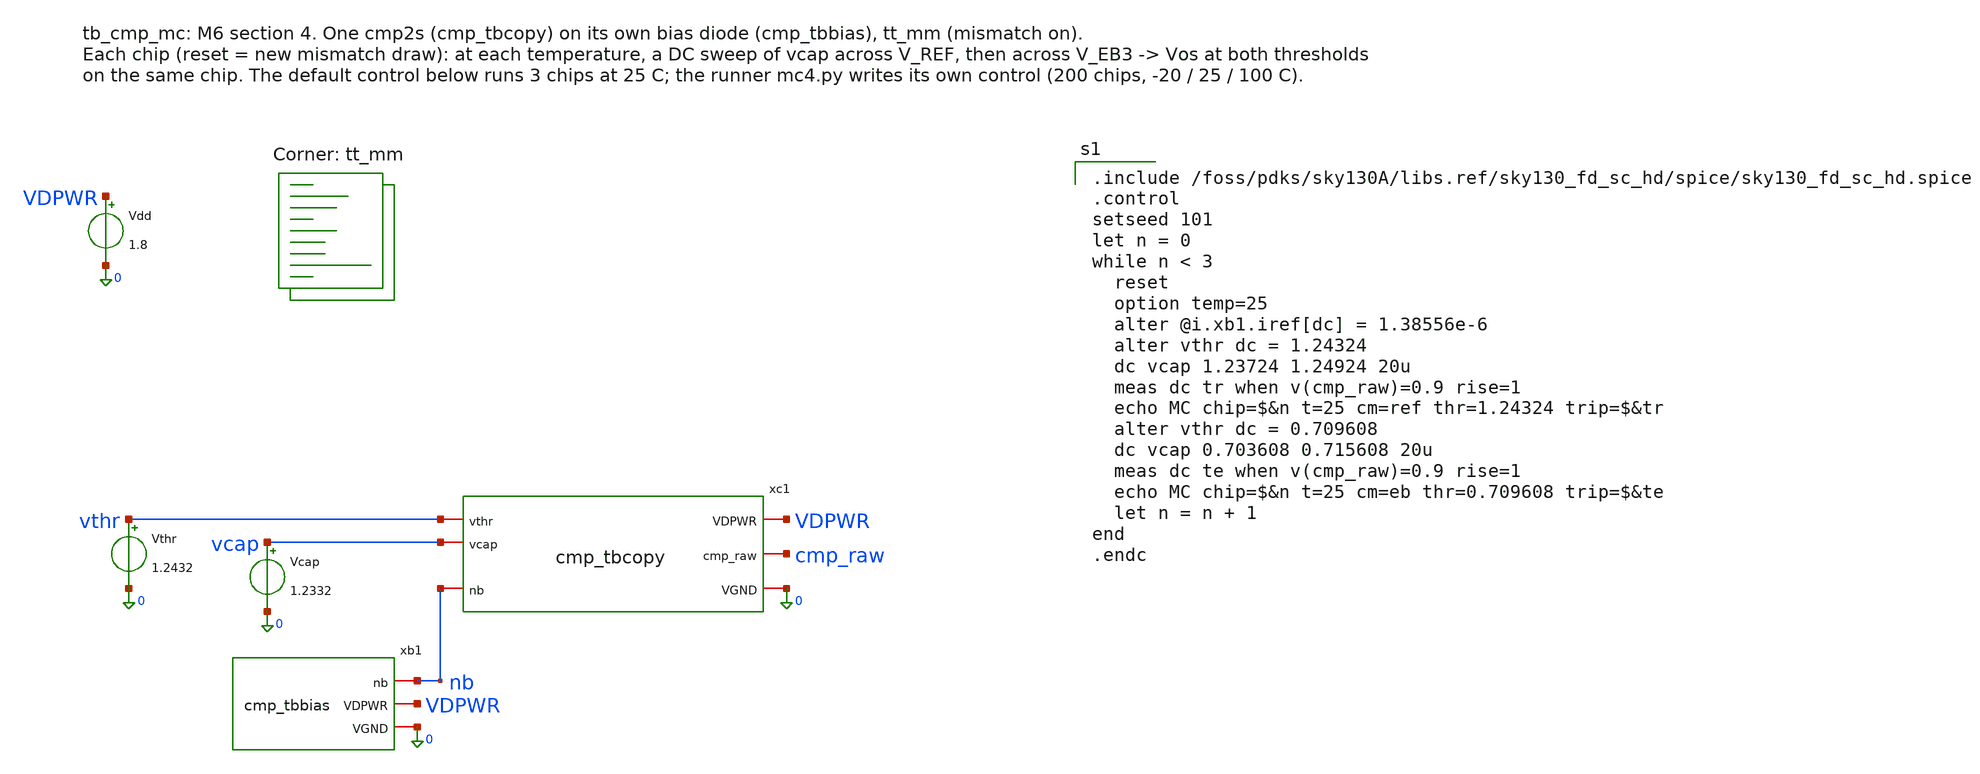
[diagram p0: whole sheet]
** sch_path: xschem/tb_cmp_mc.sch
**.subckt tb_cmp_mc
xc1 vthr vcap nb VDPWR cmp_raw 0 cmp_tbcopy
xb1 nb VDPWR 0 cmp_tbbias
Vthr vthr 0 1.2432
Vcap vcap 0 1.2332
Vdd VDPWR 0 1.8
**** begin user architecture code
.lib $::SKYWATER_MODELS/sky130.lib.spice tt_mm

.include /foss/pdks/sky130A/libs.ref/sky130_fd_sc_hd/spice/sky130_fd_sc_hd.spice
.control
setseed 101
let n = 0
while n < 3
  reset
  option temp=25
  alter @i.xb1.iref[dc] = 1.38556e-6
  alter vthr dc = 1.24324
  dc vcap 1.23724 1.24924 20u
  meas dc tr when v(cmp_raw)=0.9 rise=1
  echo MC chip=$&n t=25 cm=ref thr=1.24324 trip=$&tr
  alter vthr dc = 0.709608
  dc vcap 0.703608 0.715608 20u
  meas dc te when v(cmp_raw)=0.9 rise=1
  echo MC chip=$&n t=25 cm=eb thr=0.709608 trip=$&te
  let n = n + 1
end
.endc

**** end user architecture code
**.ends

* expanding   symbol:  cmp_tbcopy.sym # of pins=6
** sym_path: xschem/cmp_tbcopy.sym
** sch_path: xschem/cmp_tbcopy.sch
.subckt cmp_tbcopy vthr vcap nb VDPWR cmp_raw VGND
*.ipin vthr
*.ipin vcap
*.iopin nb
*.iopin VDPWR
*.opin cmp_raw
*.iopin VGND
x1 vthr vcap ib_cmp1 ib_cmp2 VDPWR cmp_raw VGND cmp2s
XMNB3 ib_cmp1 nb VGND VGND sky130_fd_pr__nfet_01v8 L=8 W=4 nf=1 ad='int((1 + 1)/2) * 4 / 1 * 0.29' as='int((1 + 2)/2) * 4 / 1 * 0.29'
+ pd='2*int((1 + 1)/2) * (4 / 1 + 0.29)' ps='2*int((1 + 2)/2) * (4 / 1 + 0.29)' nrd='0.29 / 4 ' nrs='0.29 / 4 '
+ sa=0 sb=0 sd=0 mult=4 m=4
XMNB4 ib_cmp2 nb VGND VGND sky130_fd_pr__nfet_01v8 L=8 W=4 nf=1 ad='int((1 + 1)/2) * 4 / 1 * 0.29' as='int((1 + 2)/2) * 4 / 1 * 0.29'
+ pd='2*int((1 + 1)/2) * (4 / 1 + 0.29)' ps='2*int((1 + 2)/2) * (4 / 1 + 0.29)' nrd='0.29 / 4 ' nrs='0.29 / 4 '
+ sa=0 sb=0 sd=0 mult=4 m=4
Cw1 ib_cmp1 VGND 40f m=1
Cw2 ib_cmp2 VGND 40f m=1
.ends


* expanding   symbol:  cmp_tbbias.sym # of pins=3
** sym_path: xschem/cmp_tbbias.sym
** sch_path: xschem/cmp_tbbias.sch
.subckt cmp_tbbias nb VDPWR VGND
*.iopin VDPWR
*.iopin nb
*.iopin VGND
Iref VDPWR nb 1.386u
XMNB1 nb nb VGND VGND sky130_fd_pr__nfet_01v8 L=8 W=4 nf=1 ad='int((1 + 1)/2) * 4 / 1 * 0.29' as='int((1 + 2)/2) * 4 / 1 * 0.29'
+ pd='2*int((1 + 1)/2) * (4 / 1 + 0.29)' ps='2*int((1 + 2)/2) * (4 / 1 + 0.29)' nrd='0.29 / 4 ' nrs='0.29 / 4 '
+ sa=0 sb=0 sd=0 mult=1 m=1
.ends


* expanding   symbol:  cmp2s.sym # of pins=7
** sym_path: xschem/cmp2s.sym
** sch_path: xschem/cmp2s.sch
.subckt cmp2s vthr vcap ib_cmp1 ib_cmp2 VDPWR cmp_raw VGND
*.iopin VDPWR
*.iopin VGND
*.ipin vthr
*.ipin vcap
*.iopin ib_cmp1
*.iopin ib_cmp2
*.opin cmp_raw
XM2a nd nd VDPWR VDPWR sky130_fd_pr__pfet_01v8_lvt L=4 W=4 nf=1 ad='int((1 + 1)/2) * 4 / 1 * 0.29' as='int((1 + 2)/2) * 4 / 1 * 0.29'
+ pd='2*int((1 + 1)/2) * (4 / 1 + 0.29)' ps='2*int((1 + 2)/2) * (4 / 1 + 0.29)' nrd='0.29 / 4 ' nrs='0.29 / 4 '
+ sa=0 sb=0 sd=0 mult=8 m=8
XM2b n1 nd VDPWR VDPWR sky130_fd_pr__pfet_01v8_lvt L=4 W=4 nf=1 ad='int((1 + 1)/2) * 4 / 1 * 0.29' as='int((1 + 2)/2) * 4 / 1 * 0.29'
+ pd='2*int((1 + 1)/2) * (4 / 1 + 0.29)' ps='2*int((1 + 2)/2) * (4 / 1 + 0.29)' nrd='0.29 / 4 ' nrs='0.29 / 4 '
+ sa=0 sb=0 sd=0 mult=8 m=8
XM1a nd vthr ib_cmp1 VGND sky130_fd_pr__nfet_01v8_lvt L=1.75 W=10 nf=1 ad='int((1 + 1)/2) * 10 / 1 * 0.29'
+ as='int((1 + 2)/2) * 10 / 1 * 0.29' pd='2*int((1 + 1)/2) * (10 / 1 + 0.29)' ps='2*int((1 + 2)/2) * (10 / 1 + 0.29)'
+ nrd='0.29 / 10 ' nrs='0.29 / 10 ' sa=0 sb=0 sd=0 mult=6 m=6
XM1b n1 vcap ib_cmp1 VGND sky130_fd_pr__nfet_01v8_lvt L=1.75 W=10 nf=1 ad='int((1 + 1)/2) * 10 / 1 * 0.29'
+ as='int((1 + 2)/2) * 10 / 1 * 0.29' pd='2*int((1 + 1)/2) * (10 / 1 + 0.29)' ps='2*int((1 + 2)/2) * (10 / 1 + 0.29)'
+ nrd='0.29 / 10 ' nrs='0.29 / 10 ' sa=0 sb=0 sd=0 mult=6 m=6
XM3 ib_cmp2 n1 VDPWR VDPWR sky130_fd_pr__pfet_01v8_lvt L=1 W=4 nf=1 ad='int((1 + 1)/2) * 4 / 1 * 0.29'
+ as='int((1 + 2)/2) * 4 / 1 * 0.29' pd='2*int((1 + 1)/2) * (4 / 1 + 0.29)' ps='2*int((1 + 2)/2) * (4 / 1 + 0.29)'
+ nrd='0.29 / 4 ' nrs='0.29 / 4 ' sa=0 sb=0 sd=0 mult=3 m=3
XMIP x ib_cmp2 VDPWR VDPWR sky130_fd_pr__pfet_01v8 L=1 W=0.42 nf=1 ad='int((1 + 1)/2) * 0.42 / 1 * 0.29'
+ as='int((1 + 2)/2) * 0.42 / 1 * 0.29' pd='2*int((1 + 1)/2) * (0.42 / 1 + 0.29)' ps='2*int((1 + 2)/2) * (0.42 / 1 + 0.29)'
+ nrd='0.29 / 0.42 ' nrs='0.29 / 0.42 ' sa=0 sb=0 sd=0 mult=1 m=1
XMIN x ib_cmp2 VGND VGND sky130_fd_pr__nfet_01v8 L=0.15 W=2 nf=1 ad='int((1 + 1)/2) * 2 / 1 * 0.29' as='int((1 + 2)/2) * 2 / 1 * 0.29'
+ pd='2*int((1 + 1)/2) * (2 / 1 + 0.29)' ps='2*int((1 + 2)/2) * (2 / 1 + 0.29)' nrd='0.29 / 2 ' nrs='0.29 / 2 '
+ sa=0 sb=0 sd=0 mult=1 m=1
xinv x VGND VGND VDPWR VDPWR cmp_raw sky130_fd_sc_hd__inv_1
.ends

.end
